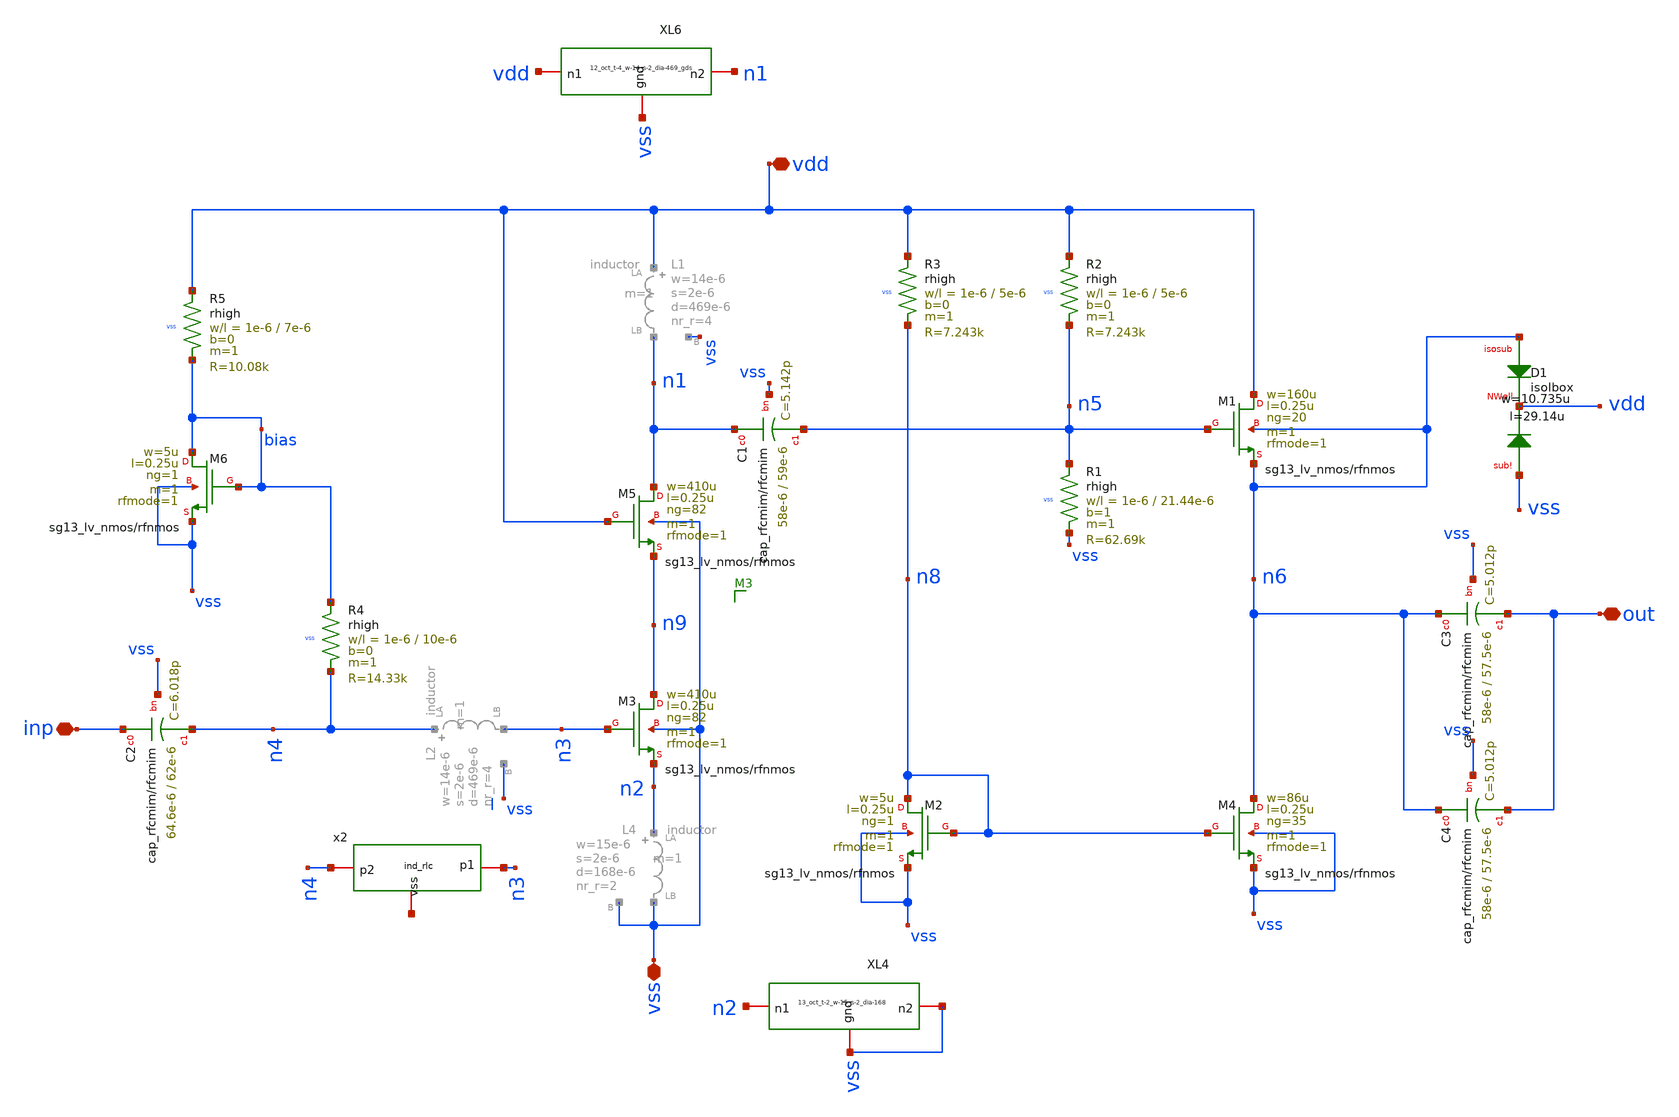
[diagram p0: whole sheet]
** sch_path: LNA7096-main/schematic/xschem/01_lna/LNA_with_buff_rlc.sch
**.subckt LNA_with_buff_rlc vdd vss inp out
*.iopin vdd
*.iopin vss
*.iopin inp
*.iopin out
XR1 n5 vss vss rhigh w=1e-6 l=21.44e-6 m=1 b=1 mm_ok=1
XR2 vdd n5 vss rhigh w=1e-6 l=5e-6 m=1 b=0 mm_ok=1
XR3 vdd n8 vss rhigh w=1e-6 l=5e-6 m=1 b=0 mm_ok=1
XR4 bias n4 vss rhigh w=1e-6 l=10e-6 m=1 b=0 mm_ok=1
XR5 vdd bias vss rhigh w=1e-6 l=7e-6 m=1 b=0 mm_ok=1
XC1 n1 n5 vss cap_rfcmim w=58e-6 l=59e-6 wfeed=5.0e-6 m=1 mm_ok=1
XC3 n6 out vss cap_rfcmim w=58e-6 l=57.5e-6 wfeed=5.0e-6 m=1 mm_ok=1
XC2 inp n4 vss cap_rfcmim w=64.6e-6 l=62e-6 wfeed=5.0e-6 m=1 mm_ok=1
XC4 n6 out vss cap_rfcmim w=58e-6 l=57.5e-6 wfeed=5.0e-6 m=1 mm_ok=1
XM5 n1 vdd n9 vss sg13_lv_nmos w=410u l=0.25u ng=82 m=1 rfmode=1 mm_ok=1
XM3 n9 n3 n2 vss sg13_lv_nmos w=410u l=0.25u ng=82 m=1 rfmode=1 mm_ok=1
XM2 n8 n8 vss vss sg13_lv_nmos w=5u l=0.25u ng=1 m=1 rfmode=1 mm_ok=1
XM4 n6 n8 vss vss sg13_lv_nmos w=86u l=0.25u ng=35 m=1 rfmode=1 mm_ok=1
XM1 vdd n5 n6 n6 sg13_lv_nmos w=160u l=0.25u ng=20 m=1 rfmode=1 mm_ok=1
XM6 bias bias vss vss sg13_lv_nmos w=5u l=0.25u ng=1 m=1 rfmode=1 mm_ok=1
x2 n4 n3 net2 ind_rlc Lser=18.1n Rser=9.8 Cshunt1=61.6f Rshunt1=2696 Cshunt2=62.2f Rshunt2=2774
XL6 vdd n1 vss 12_oct_t-4_w-14_s-2_dia-469_gds
XL4 n2 vss vss 13_oct_t-2_w-15_s-2_dia-168
XD1 n6 vdd vss isolbox l=29.14u w=10.735u
**.ends

* expanding   symbol:  01_lna/ind_rlc.sym # of pins=3
** sym_path: LNA7096-main/schematic/xschem/01_lna/ind_rlc.sym
** sch_path: LNA7096-main/schematic/xschem/01_lna/ind_rlc.sch
.subckt ind_rlc p2 p1 vss  Lser=1n Rser=1k Rshunt1=1k Cshunt1=2p Rshunt2=1k Cshunt2=2p
*.iopin p1
*.iopin p2
*.iopin vss
L1 net2 p1 'Lser' m=1
R1 net2 p2 'Rser' m=1
R2 p1 net1 'Rshunt1' m=1
C1 net1 vss 'Cshunt1' m=1
R5 p2 net3 'Rshunt2' m=1
C4 net3 vss 'Cshunt2' m=1
.ends


* expanding   symbol:  01_lna/12_oct_t-4_w-14_s-2_dia-469_gds.sym # of pins=3
** sym_path: LNA7096-main/schematic/xschem/01_lna/ind_lg.sym
.include /home/ic_design_trg/lna_ihp/xschem/01_lna/lna_pads/simulation/ngspice_s2p/12_oct_t-4_w-14_s-2_dia-469_gds.inc

* expanding   symbol:  01_lna/13_oct_t-2_w-15_s-2_dia-168.sym # of pins=3
** sym_path: LNA7096-main/schematic/xschem/01_lna/ind_lg.sym
.include /home/ic_design_trg/lna_ihp/xschem/01_lna/lna_pads/simulation/ngspice_s2p/13_oct_t-2_w-15_s-2_dia-168.inc
.end
